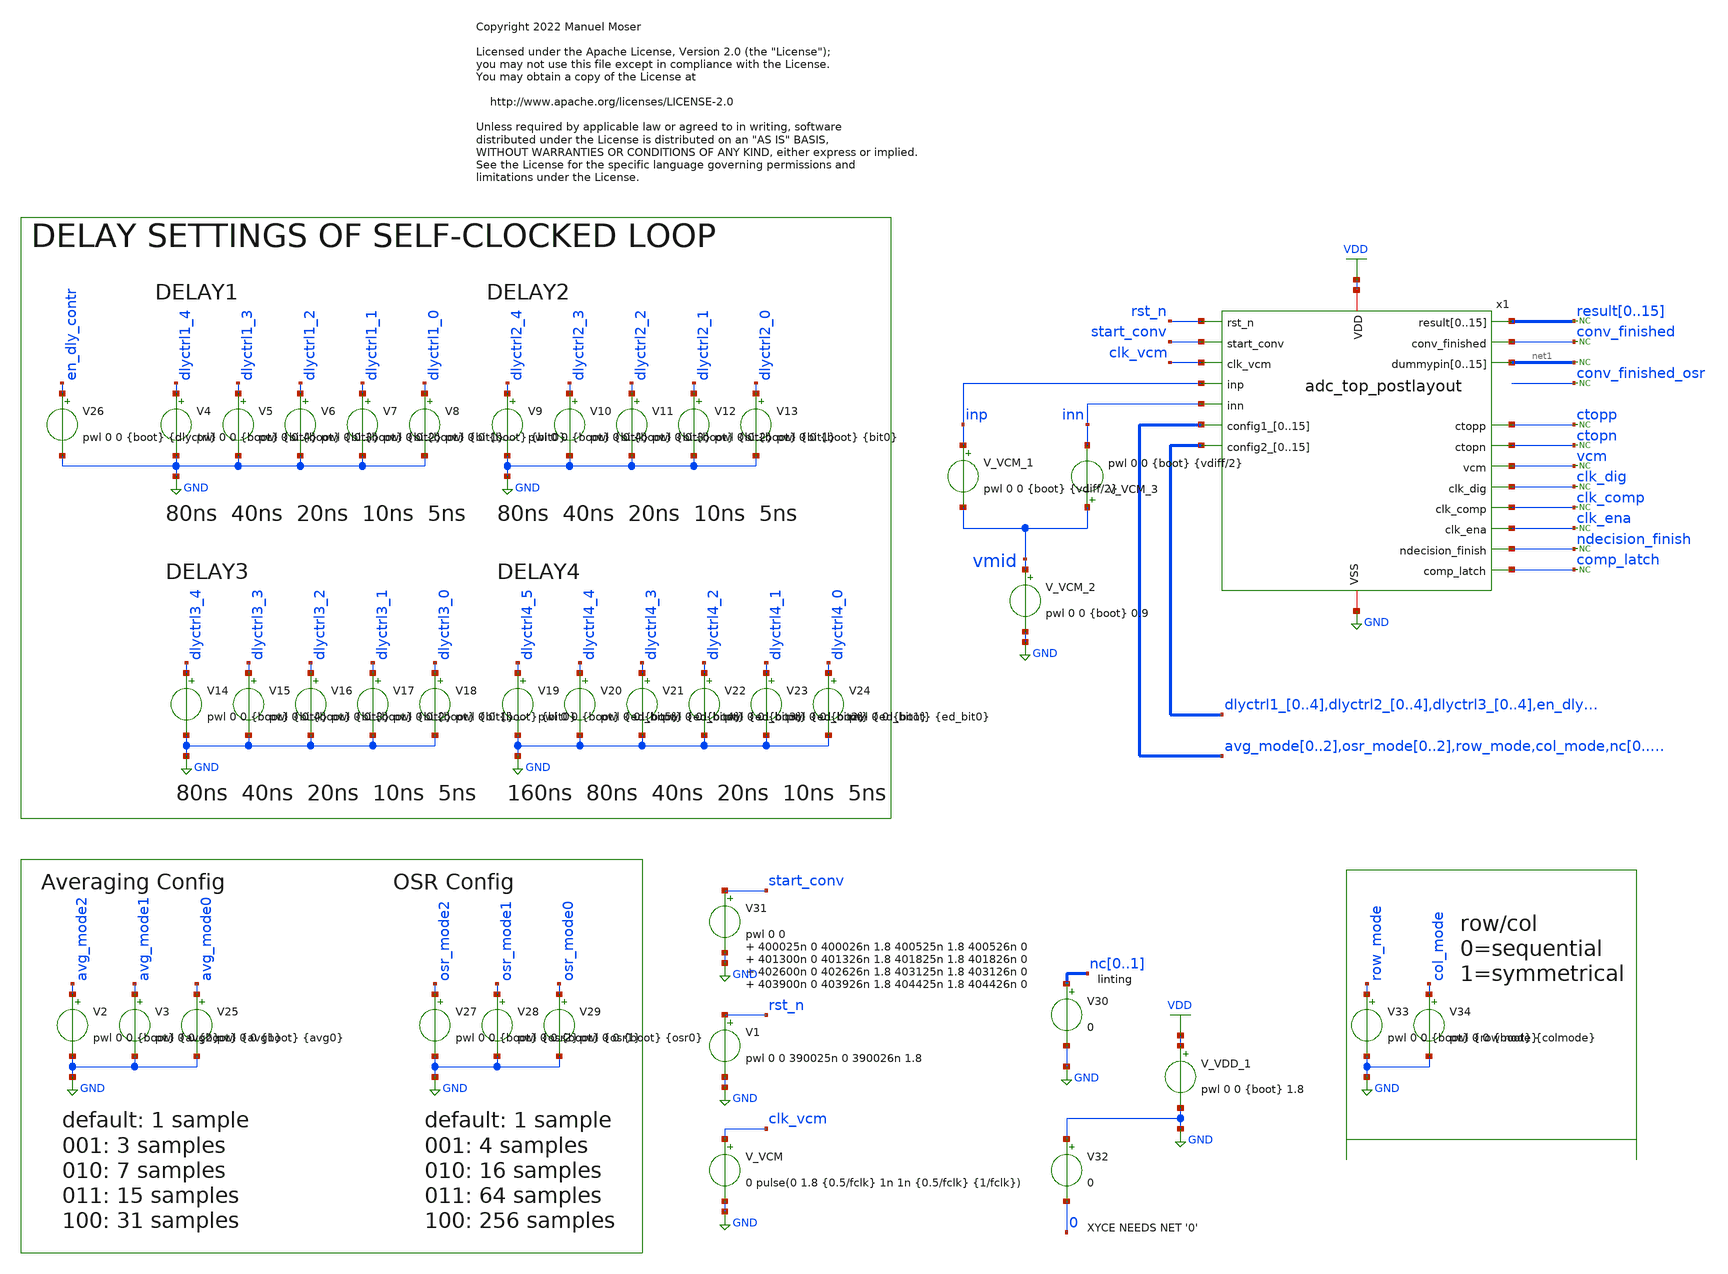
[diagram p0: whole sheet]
** sch_path: xschem/adc_top_postlayout_tb.sch
* Copyright 2022 Manuel Moser
* Licensed under the Apache License, Version 2.0 (the "License");
**.subckt adc_top_postlayout_tb
V_VDD_1 VDD GND pwl 0 0 {boot} 1.8
V_VCM_2 vmid GND pwl 0 0 {boot} 0.9
* noconn result[0..15]
* noconn conv_finished
V_VCM_1 inp vmid pwl 0 0 {boot} {vdiff/2}
V_VCM_3 vmid inn pwl 0 0 {boot} {vdiff/2}
V_VCM clk_vcm GND 0 pulse(0 1.8 {0.5/fclk} 1n 1n {0.5/fclk} {1/fclk})
V1 rst_n GND pwl 0 0 390025n 0 390026n 1.8
V31 start_conv GND pwl 0 0 400025n 0 400026n 1.8 400525n 1.8 400526n 0 401300n 0 401326n 1.8 401825n
+ 1.8 401826n 0 402600n 0 402626n 1.8 403125n 1.8 403126n 0 403900n 0 403926n 1.8 404425n 1.8 404426n 0
V4 dlyctrl1_4 GND pwl 0 0 {boot} {bit4}
V5 dlyctrl1_3 GND pwl 0 0 {boot} {bit3}
V6 dlyctrl1_2 GND pwl 0 0 {boot} {bit2}
V7 dlyctrl1_1 GND pwl 0 0 {boot} {bit1}
V8 dlyctrl1_0 GND pwl 0 0 {boot} {bit0}
V2 avg_mode2 GND pwl 0 0 {boot} {avg2}
V3 avg_mode1 GND pwl 0 0 {boot} {avg1}
V25 avg_mode0 GND pwl 0 0 {boot} {avg0}
V19 dlyctrl4_5 GND pwl 0 0 {boot} {ed_bit5}
V20 dlyctrl4_4 GND pwl 0 0 {boot} {ed_bit4}
V21 dlyctrl4_3 GND pwl 0 0 {boot} {ed_bit3}
V22 dlyctrl4_2 GND pwl 0 0 {boot} {ed_bit2}
V23 dlyctrl4_1 GND pwl 0 0 {boot} {ed_bit1}
V24 dlyctrl4_0 GND pwl 0 0 {boot} {ed_bit0}
V26 en_dly_contr GND pwl 0 0 {boot} {dlyctrl}
V27 osr_mode2 GND pwl 0 0 {boot} {osr2}
V28 osr_mode1 GND pwl 0 0 {boot} {osr1}
V29 osr_mode0 GND pwl 0 0 {boot} {osr0}
V30 nc0 GND 0
x1 result0 result1 result2 result3 result4 result5 result6 result7 result8 result9 result10 result11
+ result12 result13 result14 result15 VDD GND conv_finished rst_n start_conv clk_vcm inp inn avg_mode0
+ avg_mode1 avg_mode2 osr_mode0 osr_mode1 osr_mode2 row_mode col_mode nc0 nc1 dlyctrl4_0 dlyctrl4_1 dlyctrl4_2
+ dlyctrl4_3 dlyctrl4_4 dlyctrl4_5 dlyctrl1_0 dlyctrl1_1 dlyctrl1_2 dlyctrl1_3 dlyctrl1_4 dlyctrl2_0 dlyctrl2_1
+ dlyctrl2_2 dlyctrl2_3 dlyctrl2_4 dlyctrl3_0 dlyctrl3_1 dlyctrl3_2 dlyctrl3_3 dlyctrl3_4 en_dly_contr net1[15]
+ net1[14] net1[13] net1[12] net1[11] net1[10] net1[9] net1[8] net1[7] net1[6] net1[5] net1[4] net1[3] net1[2]
+ net1[1] net1[0] ctopp ctopn vcm clk_dig clk_comp clk_ena ndecision_finish comp_latch adc_top_postlayout
* noconn #net1
V9 dlyctrl2_4 GND pwl 0 0 {boot} {bit4}
V10 dlyctrl2_3 GND pwl 0 0 {boot} {bit3}
V11 dlyctrl2_2 GND pwl 0 0 {boot} {bit2}
V12 dlyctrl2_1 GND pwl 0 0 {boot} {bit1}
V13 dlyctrl2_0 GND pwl 0 0 {boot} {bit0}
V14 dlyctrl3_4 GND pwl 0 0 {boot} {bit4}
V15 dlyctrl3_3 GND pwl 0 0 {boot} {bit3}
V16 dlyctrl3_2 GND pwl 0 0 {boot} {bit2}
V17 dlyctrl3_1 GND pwl 0 0 {boot} {bit1}
V18 dlyctrl3_0 GND pwl 0 0 {boot} {bit0}
V32 GND 0 0
* noconn ctopp
* noconn ctopn
* noconn vcm
* noconn clk_dig
* noconn clk_comp
* noconn clk_ena
* noconn ndecision_finish
* noconn comp_latch
V33 row_mode GND pwl 0 0 {boot} {rowmode}
V34 col_mode GND pwl 0 0 {boot} {colmode}
* noconn conv_finished_osr
**** begin user architecture code

** opencircuitdesign pdks install
.lib $::SKYWATER_MODELS/sky130.lib.spice tt








* ngspice commands
.include /foss/designs/SKY130_SAR-ADC1/spice/adc_top.gds.C.noD.merge.postlayout.spice
.include /foss/pdks/sky130A/libs.ref/sky130_fd_sc_hd/spice/sky130_fd_sc_hd.spice

****************
* Misc
****************
.param fclk=32768
.param vdiff=200m
.param boot=1u

****************
* Delay Config
****************
.param dlyctrl = 1.8

* delay 1-3
.param bit0 = 0
.param bit1 = 1.8
.param bit2 = 0
.param bit3 = 0
.param bit4 = 0

* edgedetect pulse
.param ed_bit0 = 0
.param ed_bit1 = 0
.param ed_bit2 = 1.8
.param ed_bit3 = 1.8
.param ed_bit4 = 0
.param ed_bit5 = 0

****************
* Averaging Config
****************
.param avg0 = 0
.param avg1 = 0
.param avg2 = 0

****************
* OSR Config
****************
.param osr0 = 0
.param osr1 = 0
.param osr2 = 0


.save all
.control
set num_threads=11
tran 50n 650u
plot inp inn rst_n start_conv conv_finished
plot start_conv x1.clk_dig x1.clk_comp
plot x1.pctop x1.nctop x1.comparator_result
plot x1.pctop-x1.nctop

let k = length(time) - 1

* Print the result vector at the end of tran
print result15[k] result14[k] result13[k] result12[k] result11[k] result10[k] result9[k] result8[k]
+ result7[k] result6[k] result5[k] result4[k] result3[k] result2[k] result1[k] result0[k]
* Print the result diff-voltage at the end of tran
print
+ ((result15[k]*2048+result14[k]*1024+result13[k]*512+result12[k]*256+result11[k]*128+result10[k]*64+result9[k]*32+result8[k]*16+result7[k]*8+result6[k]*4+result5[k]*2+result4[k]*1+result3[k]*0.5+result2[k]*0.25+result1[k]*0.125+result0[k]*0.0625)-2048*1.8)/2048
.endc



**** end user architecture code
**.ends
.GLOBAL VDD
.GLOBAL GND
.end
